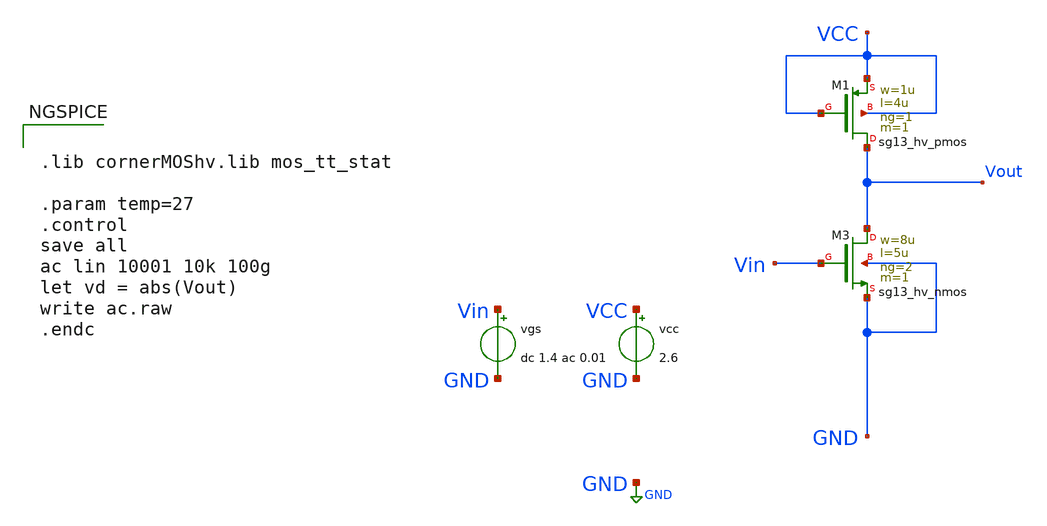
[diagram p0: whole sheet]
** sch_path: lectures/2025-08-28/ac.sch
**.subckt ac
vcc VCC GND 2.6
XM3 Vout Vin GND GND sg13_hv_nmos w=8u l=5u ng=2 m=1 mm_ok=1
XM1 Vout VCC VCC VCC sg13_hv_pmos w=1u l=4u ng=1 m=1 mm_ok=1
vgs Vin GND dc 1.4 ac 0.01
**** begin user architecture code


.lib cornerMOShv.lib mos_tt_stat

.param temp=27
.control
save all
ac lin 10001 10k 100g
let vd = abs(Vout)
write ac.raw
.endc


**** end user architecture code
**.ends
.GLOBAL GND
.end
